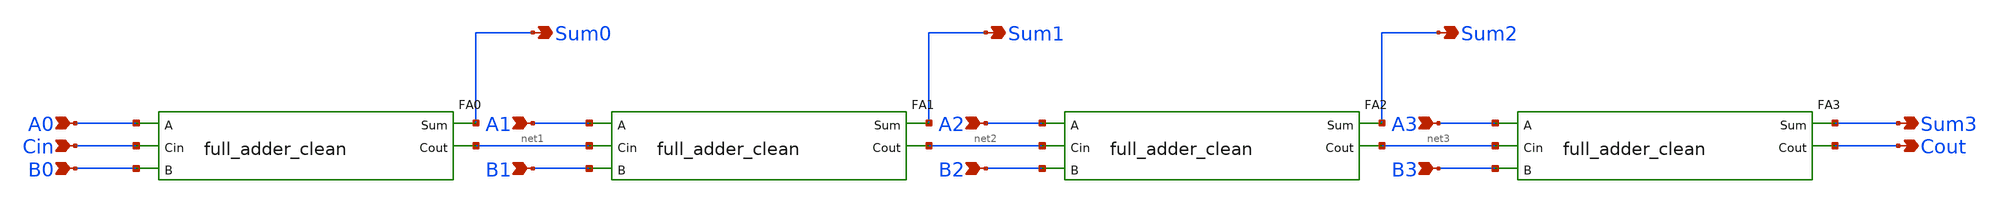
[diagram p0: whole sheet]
** sch_path: xschem/adder_4bit.sch
**.subckt adder_4bit A0 B0 Cin A1 B1 A2 B2 A3 B3 Sum0 Sum1 Sum2 Sum3 Cout
*.ipin A0
*.ipin B0
*.ipin Cin
*.ipin A1
*.ipin B1
*.ipin A2
*.ipin B2
*.ipin A3
*.ipin B3
*.opin Sum0
*.opin Sum1
*.opin Sum2
*.opin Sum3
*.opin Cout
FA0 A0 Sum0 Cin B0 net1 full_adder_clean
FA1 A1 Sum1 net1 B1 net2 full_adder_clean
FA2 A2 Sum2 net2 B2 net3 full_adder_clean
FA3 A3 Sum3 net3 B3 Cout full_adder_clean
**.ends

* expanding   symbol:  full_adder_clean.sym # of pins=5
** sym_path: xschem/full_adder_clean.sym
** sch_path: xschem/full_adder_clean.sch
.subckt full_adder_clean A Sum Cin B Cout
*.ipin A
*.ipin B
*.ipin Cin
*.opin Sum
*.opin Cout
x1 A B VGND VNB VPB VPWR P sky130_fd_sc_hd__xor2_1
x2 P Cin VGND VNB VPB VPWR Sum sky130_fd_sc_hd__xor2_1
x3 A B VGND VNB VPB VPWR G1 sky130_fd_sc_hd__and2_1
x4 P Cin VGND VNB VPB VPWR G2 sky130_fd_sc_hd__and2_1
x5 G1 G2 VGND VNB VPB VPWR Cout sky130_fd_sc_hd__or2_1
.ends

.end
